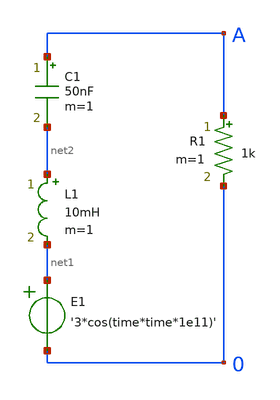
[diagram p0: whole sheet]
** sch_path: designs/.config/rlc.sch
**.subckt rlc
C1 A net2 50nF m=1
R1 A 0 1k m=1
L1 net2 net1 10mH m=1
E1 net1 0 VOL=' '3*cos(time*time*1e11)' '
**** begin user architecture code


.tran 10n 2000u uic
.save all


**** end user architecture code
**.ends
.end
